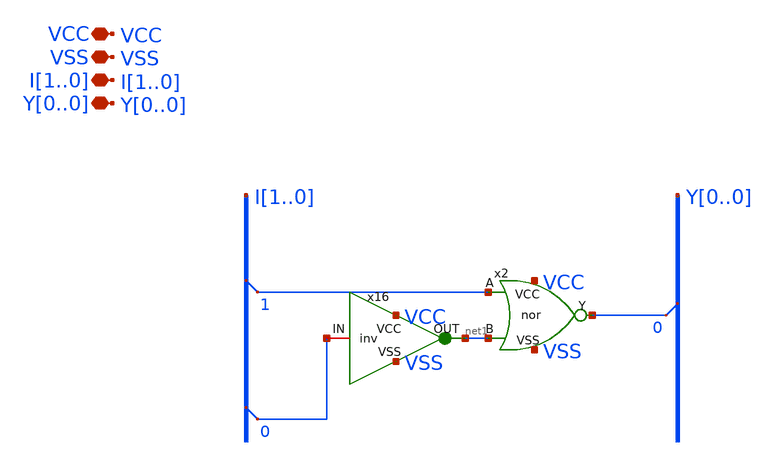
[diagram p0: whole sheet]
** sch_path: peripherals/priority_selector2.sch
**.subckt priority_selector2 I1,I0 Y0 VSS VCC
*.iopin I1,I0
*.iopin Y0
*.iopin VSS
*.iopin VCC
* tap: I[1..0] --> I1
x2 VCC Y0 I1 net1 VSS nor
x16 VCC I0 net1 VSS inv
* tap: I[1..0] --> I0
* tap: Y[0..0] --> Y0
**.ends

* expanding   symbol:  logic gates/nor.sym # of pins=5
** sym_path: logic gates/nor.sym
** sch_path: logic gates/nor.sch
.subckt nor VCC Y A B VSS
*.iopin VCC
*.iopin VSS
*.iopin Y
*.iopin A
*.iopin B
XM2 Y B VSS VSS sky130_fd_pr__nfet_01v8 L=0.15 W=1 nf=1 ad='int((1 + 1)/2) * 1 / 1 * 0.29' as='int((1 + 2)/2) * 1 / 1 * 0.29'
+ pd='2*int((1 + 1)/2) * (1 / 1 + 0.29)' ps='2*int((1 + 2)/2) * (1 / 1 + 0.29)' nrd='0.29 / 1 ' nrs='0.29 / 1 '
+ sa=0 sb=0 sd=0 mult=1 m=1
XM11 Y B net1 VCC sky130_fd_pr__pfet_01v8 L=0.15 W=1 nf=1 ad='int((nf+1)/2) * W/nf * 0.29' as='int((nf+2)/2) * W/nf * 0.29'
+ pd='2*int((nf+1)/2) * (W/nf + 0.29)' ps='2*int((nf+2)/2) * (W/nf + 0.29)' nrd='0.29 / W' nrs='0.29 / W'
+ sa=0 sb=0 sd=0 mult=1 m=1
XM1 Y A VSS VSS sky130_fd_pr__nfet_01v8 L=0.15 W=1 nf=1 ad='int((1 + 1)/2) * 1 / 1 * 0.29' as='int((1 + 2)/2) * 1 / 1 * 0.29'
+ pd='2*int((1 + 1)/2) * (1 / 1 + 0.29)' ps='2*int((1 + 2)/2) * (1 / 1 + 0.29)' nrd='0.29 / 1 ' nrs='0.29 / 1 '
+ sa=0 sb=0 sd=0 mult=1 m=1
XM3 net1 A VCC VCC sky130_fd_pr__pfet_01v8 L=0.15 W=1 nf=1 ad='int((nf+1)/2) * W/nf * 0.29' as='int((nf+2)/2) * W/nf * 0.29'
+ pd='2*int((nf+1)/2) * (W/nf + 0.29)' ps='2*int((nf+2)/2) * (W/nf + 0.29)' nrd='0.29 / W' nrs='0.29 / W'
+ sa=0 sb=0 sd=0 mult=1 m=1
.ends


* expanding   symbol:  inv.sym # of pins=4
** sym_path: peripherals/inv.sym
** sch_path: peripherals/inv.sch
.subckt inv VCC IN OUT VSS
*.iopin VCC
*.iopin IN
*.iopin OUT
*.iopin VSS
XM1 OUT IN VSS VSS sky130_fd_pr__nfet_01v8 L=0.15 W=0.5 nf=1 ad='int((nf+1)/2) * W/nf * 0.29' as='int((nf+2)/2) * W/nf * 0.29'
+ pd='2*int((nf+1)/2) * (W/nf + 0.29)' ps='2*int((nf+2)/2) * (W/nf + 0.29)' nrd='0.29 / W' nrs='0.29 / W'
+ sa=0 sb=0 sd=0 mult=1 m=1
XM2 OUT IN VCC VCC sky130_fd_pr__pfet_01v8 L=0.15 W=1.05 nf=1 ad='int((nf+1)/2) * W/nf * 0.29' as='int((nf+2)/2) * W/nf * 0.29'
+ pd='2*int((nf+1)/2) * (W/nf + 0.29)' ps='2*int((nf+2)/2) * (W/nf + 0.29)' nrd='0.29 / W' nrs='0.29 / W'
+ sa=0 sb=0 sd=0 mult=1 m=1
.ends

.end
